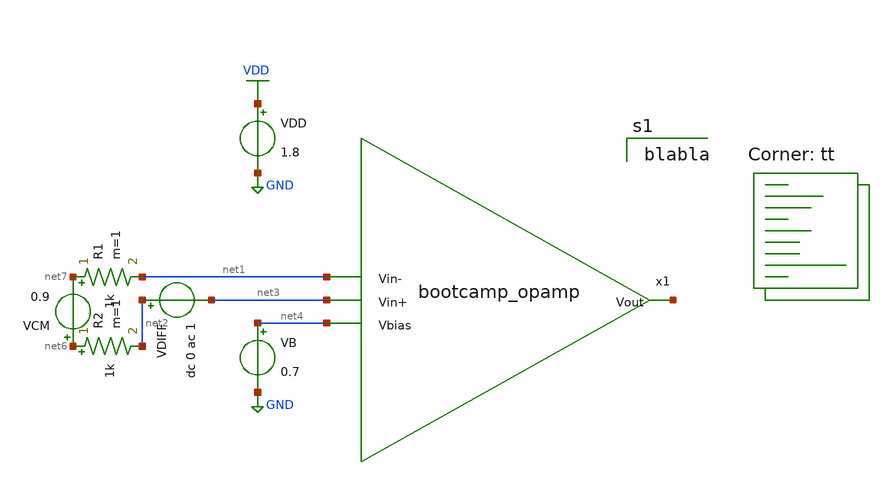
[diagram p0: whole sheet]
** sch_path: analog/schematics/tb_ac_analysis.sch
**.subckt tb_ac_analysis
x1 net5 net1 net3 net4 bootcamp_opamp
VDD VDD GND 1.8
VCM net6 net7 0.9
VB net4 GND 0.7
VDIFF net2 net3 dc 0 ac 1
R1 net7 net1 1k m=1
R2 net6 net2 1k m=1
**** begin user architecture code

blabla

.lib $::SKYWATER_MODELS/sky130.lib.spice tt
**** end user architecture code
**.ends
.GLOBAL GND
.GLOBAL VDD
.end
